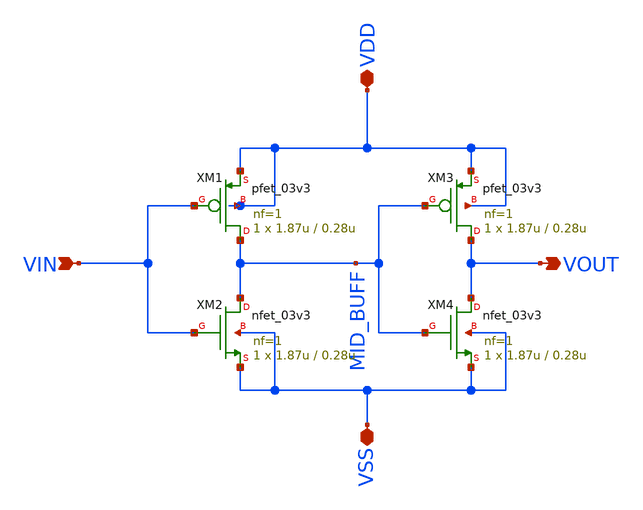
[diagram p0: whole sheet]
** sch_path: ABC123_SDC/design_data/klayout/BUFF/BUFF.sch
**.subckt BUFF VIN VDD VSS VOUT
*.ipin VIN
*.iopin VDD
*.iopin VSS
*.opin VOUT
XM1 MID_BUFF VIN VDD VDD pfet_03v3 L=0.28u W=1.87u nf=1 ad='int((nf+1)/2) * W/nf * 0.18u' as='int((nf+2)/2) * W/nf * 0.18u'
+ pd='2*int((nf+1)/2) * (W/nf + 0.18u)' ps='2*int((nf+2)/2) * (W/nf + 0.18u)' nrd='0.18u / W' nrs='0.18u / W'
+ sa=0 sb=0 sd=0 m=1
XM2 MID_BUFF VIN VSS VSS nfet_03v3 L=0.28u W=1.87u nf=1 ad='int((nf+1)/2) * W/nf * 0.18u' as='int((nf+2)/2) * W/nf * 0.18u'
+ pd='2*int((nf+1)/2) * (W/nf + 0.18u)' ps='2*int((nf+2)/2) * (W/nf + 0.18u)' nrd='0.18u / W' nrs='0.18u / W'
+ sa=0 sb=0 sd=0 m=1
XM3 VOUT MID_BUFF VDD VDD pfet_03v3 L=0.28u W=1.87u nf=1 ad='int((nf+1)/2) * W/nf * 0.18u' as='int((nf+2)/2) * W/nf * 0.18u'
+ pd='2*int((nf+1)/2) * (W/nf + 0.18u)' ps='2*int((nf+2)/2) * (W/nf + 0.18u)' nrd='0.18u / W' nrs='0.18u / W'
+ sa=0 sb=0 sd=0 m=1
XM4 VOUT MID_BUFF VSS VSS nfet_03v3 L=0.28u W=1.87u nf=1 ad='int((nf+1)/2) * W/nf * 0.18u' as='int((nf+2)/2) * W/nf * 0.18u'
+ pd='2*int((nf+1)/2) * (W/nf + 0.18u)' ps='2*int((nf+2)/2) * (W/nf + 0.18u)' nrd='0.18u / W' nrs='0.18u / W'
+ sa=0 sb=0 sd=0 m=1
**.ends
.end
